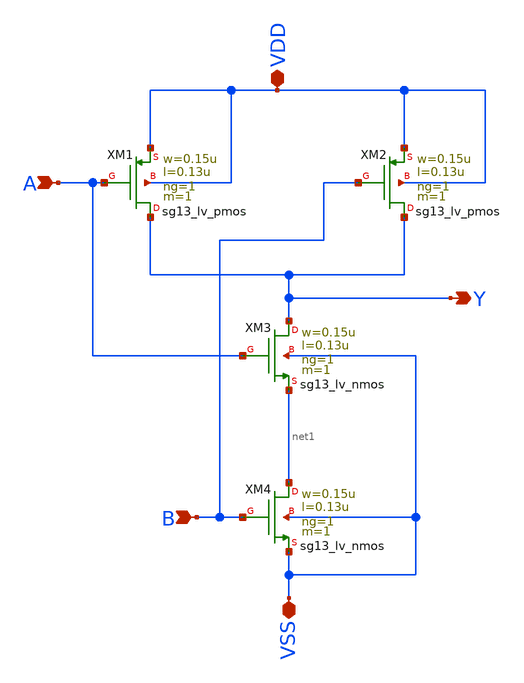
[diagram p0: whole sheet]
** sch_path: LogicGate/NAND2.sch
**.subckt NAND2 Y VDD VSS A B
*.opin Y
*.iopin VDD
*.iopin VSS
*.ipin A
*.ipin B
XXM2 Y B VDD VDD sg13_lv_pmos w=0.15u l=0.13u ng=1 m=1 mm_ok=1
XXM1 Y A VDD VDD sg13_lv_pmos w=0.15u l=0.13u ng=1 m=1 mm_ok=1
XXM3 Y A net1 VSS sg13_lv_nmos w=0.15u l=0.13u ng=1 m=1 mm_ok=1
XXM4 net1 B VSS VSS sg13_lv_nmos w=0.15u l=0.13u ng=1 m=1 mm_ok=1
**.ends
.end
